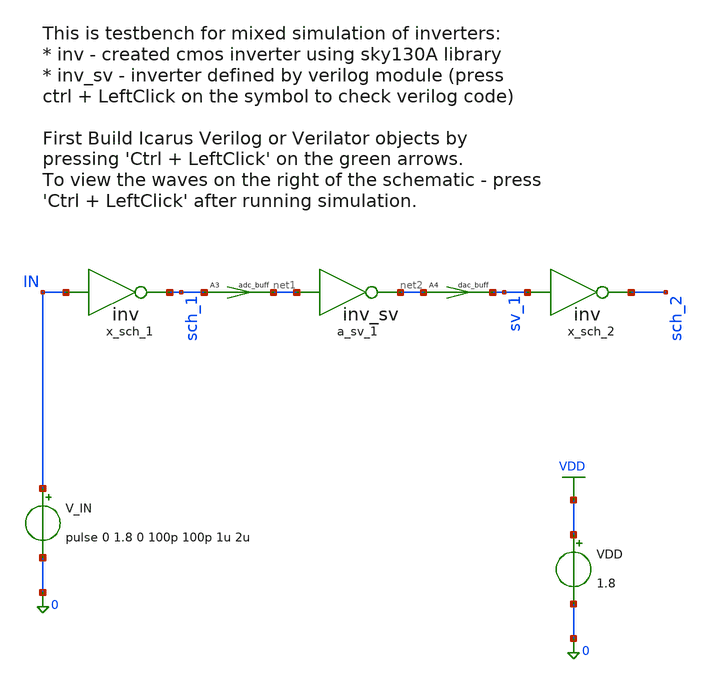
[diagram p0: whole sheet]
** sch_path: designs_backup/designs/inv_mixed/xschem/inv_test_series.sch
**.subckt inv_test_series
V_IN IN 0 pulse 0 1.8 0 100p 100p 1u 2u
VDD VDD 0 1.8
x_sch_1 IN sch_1 inv
a_sv_1 [ net1 ] [ net2 ] inv_sv
A3 [ sch_1 ] [ net1 ] adc_buff
A4 [ net2 ] [ sv_1 ] dac_buff
x_sch_2 sv_1 sch_2 inv
**** begin user architecture code

** opencircuitdesign pdks install
.lib $::SKYWATER_MODELS/sky130.lib.spice tt



.control
  save all
  tran 100p 5u
  write inv_test_series.raw
  write /foss/designs/inv_mixed/results/inv_test_series.raw
  quit
.endc


**** end user architecture code
**.ends

* expanding   symbol:  inv.sym # of pins=2
** sym_path: designs_backup/designs/inv_mixed/xschem/inv.sym
** sch_path: designs_backup/designs/inv_mixed/xschem/inv.sch
.subckt inv IN OUT
*.opin OUT
*.ipin IN
XM1 OUT IN VDD VDD sky130_fd_pr__pfet_01v8 L=0.15 W=0.42 nf=1 ad='int((1 + 1)/2) * 0.42 / 1 * 0.29' as='int((1 + 2)/2) * 0.42 / 1 * 0.29'
+ pd='2*int((1 + 1)/2) * (0.42 / 1 + 0.29)' ps='2*int((1 + 2)/2) * (0.42 / 1 + 0.29)' nrd='0.29 / 0.42 '
+ nrs='0.29 / 0.42 ' sa=0 sb=0 sd=0 mult=1 m=1
XM3 OUT IN 0 0 sky130_fd_pr__nfet_01v8 L=0.15 W=0.42 nf=1 ad='int((1 + 1)/2) * 0.42 / 1 * 0.29' as='int((1 + 2)/2) * 0.42 / 1 * 0.29'
+ pd='2*int((1 + 1)/2) * (0.42 / 1 + 0.29)' ps='2*int((1 + 2)/2) * (0.42 / 1 + 0.29)' nrd='0.29 / 0.42 '
+ nrs='0.29 / 0.42 ' sa=0 sb=0 sd=0 mult=1 m=1
.ends

.GLOBAL VDD
**** begin user architecture code
.model adc_buff adc_bridge(in_low=0.6 in_high=1.2 rise_delay=1p fall_delay=1p)
.model inv_sv d_cosim simulation="ivlng" sim_args=["inv_sv.vvp"] delay=1p
.model dac_buff dac_bridge(input_load=1e-15 t_rise=1p t_fall=1p out_low=0 out_high=1.8)
**** end user architecture code
.end
